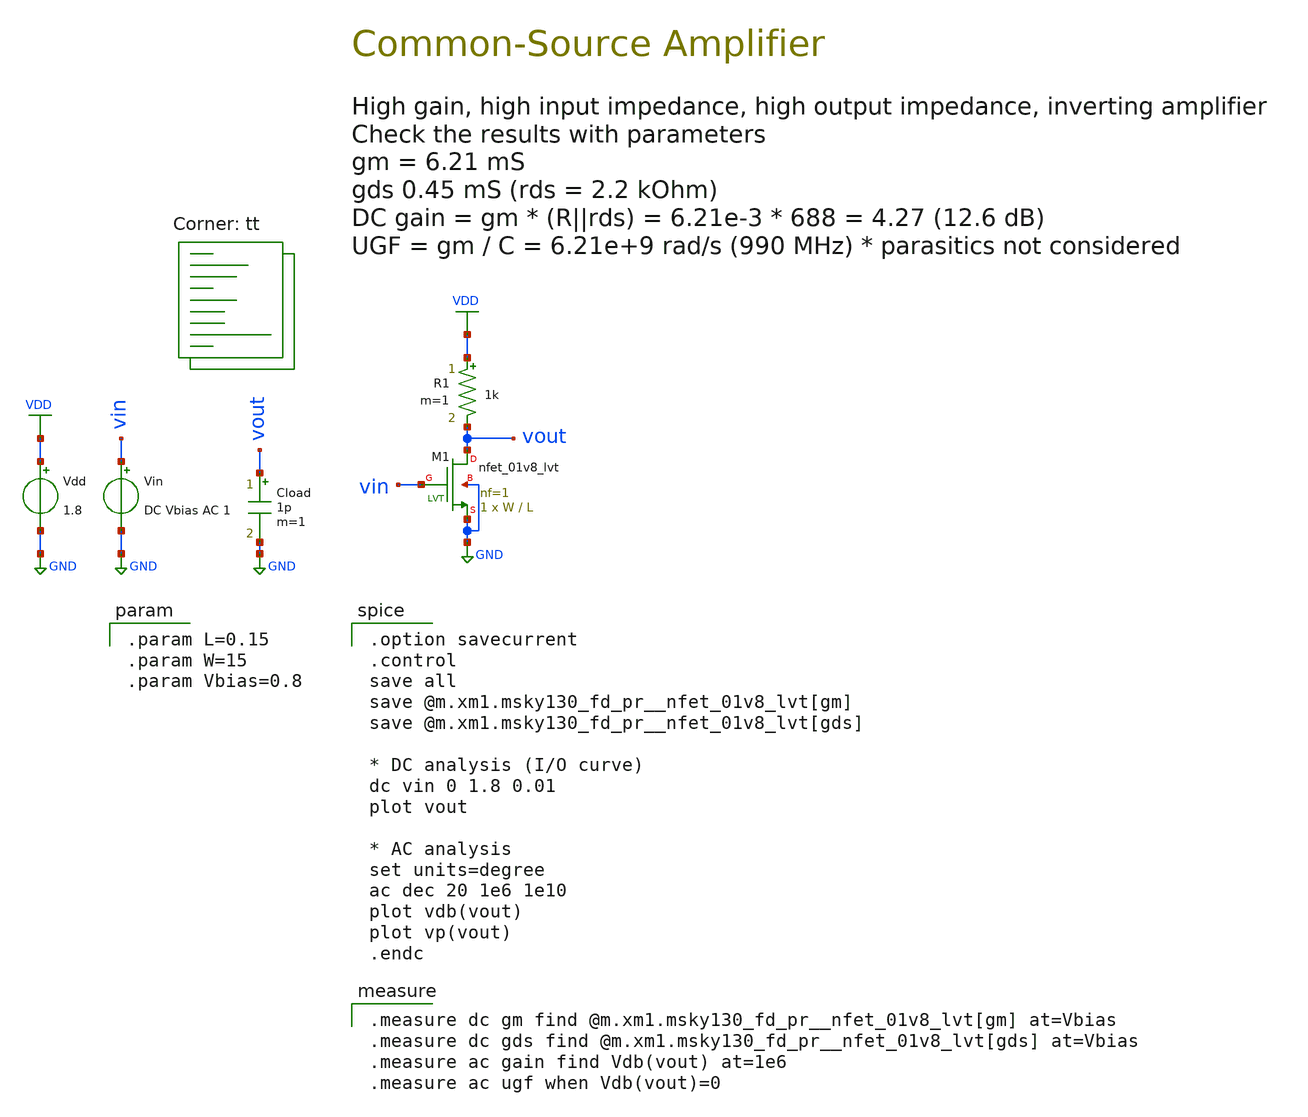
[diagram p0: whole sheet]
** sch_path: 00-g_common-source-amp.sch
**.subckt 00-g_common-source-amp
XM1 vout vin GND GND sky130_fd_pr__nfet_01v8_lvt L=L W=W nf=1 ad='int((1 + 1)/2) * W / 1 * 0.29' as='int((1 + 2)/2) * W / 1 * 0.29'
+ pd='2*int((1 + 1)/2) * (W / 1 + 0.29)' ps='2*int((1 + 2)/2) * (W / 1 + 0.29)' nrd='0.29 / W ' nrs='0.29 / W '
+ sa=0 sb=0 sd=0 mult=1 m=1
Vdd VDD GND 1.8
Vin vin GND DC Vbias AC 1
R1 VDD vout 1k m=1
Cload vout GND 1p m=1
**** begin user architecture code
.lib $::SKYWATER_MODELS/sky130.lib.spice tt

.param L=0.15
.param W=15
.param Vbias=0.8


.option savecurrent
.control
save all
save @m.xm1.msky130_fd_pr__nfet_01v8_lvt[gm]
save @m.xm1.msky130_fd_pr__nfet_01v8_lvt[gds]

* DC analysis (I/O curve)
dc vin 0 1.8 0.01
plot vout

* AC analysis
set units=degree
ac dec 20 1e6 1e10
plot vdb(vout)
plot vp(vout)
.endc


.measure dc gm find @m.xm1.msky130_fd_pr__nfet_01v8_lvt[gm] at=Vbias
.measure dc gds find @m.xm1.msky130_fd_pr__nfet_01v8_lvt[gds] at=Vbias
.measure ac gain find Vdb(vout) at=1e6
.measure ac ugf when Vdb(vout)=0

**** end user architecture code
**.ends
.GLOBAL GND
.GLOBAL VDD
.end
